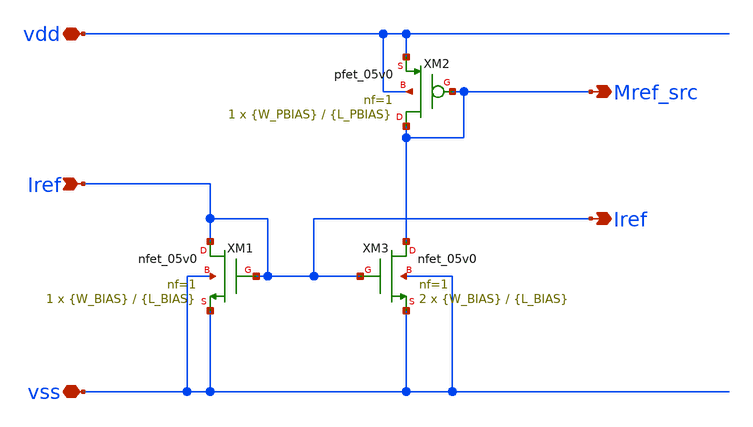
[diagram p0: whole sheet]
** sch_path: designs/libs/core_analog/iref/iref.sch
**.subckt iref Iref vdd vss Mref_src Iref
*.ipin Iref
*.iopin vdd
*.iopin vss
*.opin Mref_src
*.opin Iref
XM2 Mref_src Mref_src vdd vdd pfet_05v0 L={L_PBIAS} W={W_PBIAS} nf=1 ad='int((nf+1)/2) * W/nf * 0.18u'
+ as='int((nf+2)/2) * W/nf * 0.18u' pd='2*int((nf+1)/2) * (W/nf + 0.18u)' ps='2*int((nf+2)/2) * (W/nf + 0.18u)'
+ nrd='0.18u / W' nrs='0.18u / W' sa=0 sb=0 sd=0 m=1
XM1 Iref Iref vss vss nfet_05v0 L={L_BIAS} W={W_BIAS} nf=1 ad='int((nf+1)/2) * W/nf * 0.18u' as='int((nf+2)/2) * W/nf * 0.18u'
+ pd='2*int((nf+1)/2) * (W/nf + 0.18u)' ps='2*int((nf+2)/2) * (W/nf + 0.18u)' nrd='0.18u / W' nrs='0.18u / W'
+ sa=0 sb=0 sd=0 m=1
XM3 Mref_src Iref vss vss nfet_05v0 L={L_BIAS} W={W_BIAS} nf=1 ad='int((nf+1)/2) * W/nf * 0.18u' as='int((nf+2)/2) * W/nf * 0.18u'
+ pd='2*int((nf+1)/2) * (W/nf + 0.18u)' ps='2*int((nf+2)/2) * (W/nf + 0.18u)' nrd='0.18u / W' nrs='0.18u / W'
+ sa=0 sb=0 sd=0 m=2
**.ends
.end
